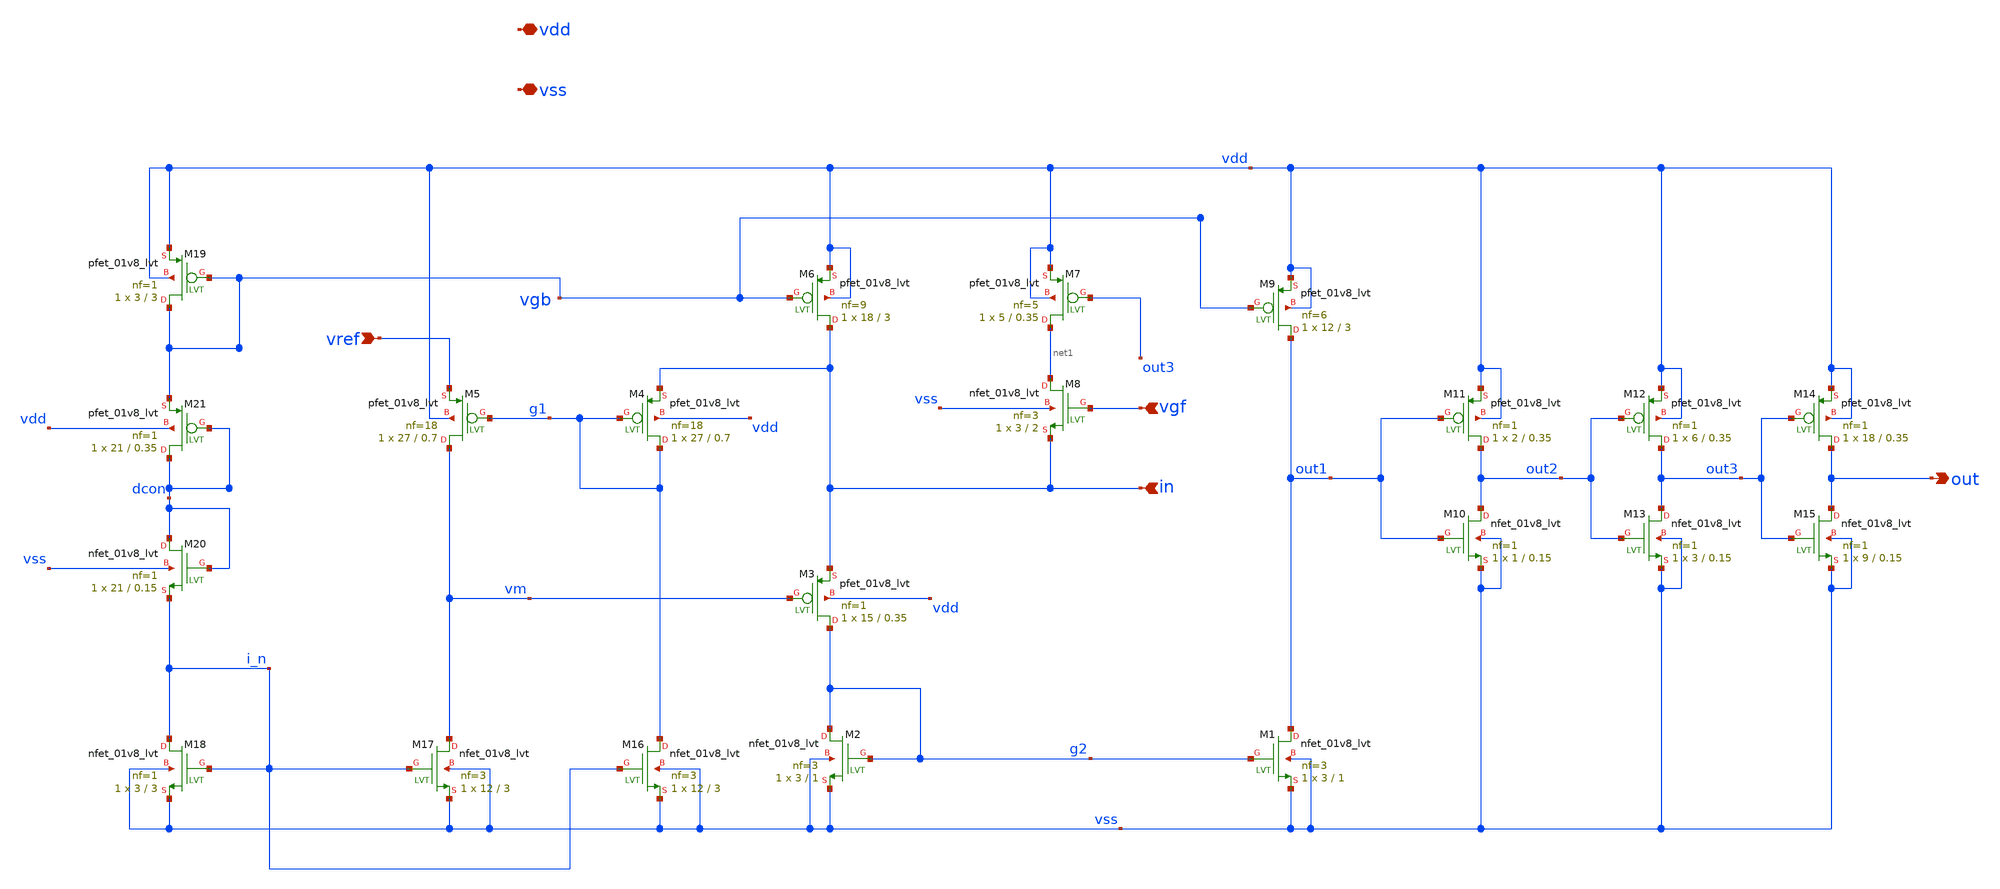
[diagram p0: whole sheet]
** sch_path: xschem/CurrentTrigger.sch
**.subckt CurrentTrigger vdd vss in out vref vgf
*.iopin vdd
*.iopin vss
*.ipin in
*.opin out
*.ipin vref
*.ipin vgf
XM1 out1 g2 vss vss sky130_fd_pr__nfet_01v8_lvt L=1 W=3 nf=3 ad='int((nf+1)/2) * W/nf * 0.29' as='int((nf+2)/2) * W/nf * 0.29'
+ pd='2*int((nf+1)/2) * (W/nf + 0.29)' ps='2*int((nf+2)/2) * (W/nf + 0.29)' nrd='0.29 / W' nrs='0.29 / W'
+ sa=0 sb=0 sd=0 mult=1 m=1
XM2 g2 g2 vss vss sky130_fd_pr__nfet_01v8_lvt L=1 W=3 nf=3 ad='int((nf+1)/2) * W/nf * 0.29' as='int((nf+2)/2) * W/nf * 0.29'
+ pd='2*int((nf+1)/2) * (W/nf + 0.29)' ps='2*int((nf+2)/2) * (W/nf + 0.29)' nrd='0.29 / W' nrs='0.29 / W'
+ sa=0 sb=0 sd=0 mult=1 m=1
XM3 g2 vm in vdd sky130_fd_pr__pfet_01v8_lvt L=0.35 W=15 nf=1 ad='int((nf+1)/2) * W/nf * 0.29' as='int((nf+2)/2) * W/nf * 0.29'
+ pd='2*int((nf+1)/2) * (W/nf + 0.29)' ps='2*int((nf+2)/2) * (W/nf + 0.29)' nrd='0.29 / W' nrs='0.29 / W'
+ sa=0 sb=0 sd=0 mult=1 m=1
XM4 g1 g1 in vdd sky130_fd_pr__pfet_01v8_lvt L=0.7 W=27 nf=18 ad='int((nf+1)/2) * W/nf * 0.29' as='int((nf+2)/2) * W/nf * 0.29'
+ pd='2*int((nf+1)/2) * (W/nf + 0.29)' ps='2*int((nf+2)/2) * (W/nf + 0.29)' nrd='0.29 / W' nrs='0.29 / W'
+ sa=0 sb=0 sd=0 mult=1 m=1
XM5 vm g1 vref vdd sky130_fd_pr__pfet_01v8_lvt L=0.7 W=27 nf=18 ad='int((nf+1)/2) * W/nf * 0.29' as='int((nf+2)/2) * W/nf * 0.29'
+ pd='2*int((nf+1)/2) * (W/nf + 0.29)' ps='2*int((nf+2)/2) * (W/nf + 0.29)' nrd='0.29 / W' nrs='0.29 / W'
+ sa=0 sb=0 sd=0 mult=1 m=1
XM6 in vgb vdd vdd sky130_fd_pr__pfet_01v8_lvt L=3 W=18 nf=9 ad='int((nf+1)/2) * W/nf * 0.29' as='int((nf+2)/2) * W/nf * 0.29'
+ pd='2*int((nf+1)/2) * (W/nf + 0.29)' ps='2*int((nf+2)/2) * (W/nf + 0.29)' nrd='0.29 / W' nrs='0.29 / W'
+ sa=0 sb=0 sd=0 mult=1 m=1
XM7 net1 out3 vdd vdd sky130_fd_pr__pfet_01v8_lvt L=0.35 W=5 nf=5 ad='int((nf+1)/2) * W/nf * 0.29' as='int((nf+2)/2) * W/nf * 0.29'
+ pd='2*int((nf+1)/2) * (W/nf + 0.29)' ps='2*int((nf+2)/2) * (W/nf + 0.29)' nrd='0.29 / W' nrs='0.29 / W'
+ sa=0 sb=0 sd=0 mult=1 m=1
XM9 out1 vgb vdd vdd sky130_fd_pr__pfet_01v8_lvt L=3 W=12 nf=6 ad='int((nf+1)/2) * W/nf * 0.29' as='int((nf+2)/2) * W/nf * 0.29'
+ pd='2*int((nf+1)/2) * (W/nf + 0.29)' ps='2*int((nf+2)/2) * (W/nf + 0.29)' nrd='0.29 / W' nrs='0.29 / W'
+ sa=0 sb=0 sd=0 mult=1 m=1
XM10 out2 out1 vss vss sky130_fd_pr__nfet_01v8_lvt L=0.15 W=1 nf=1 ad='int((nf+1)/2) * W/nf * 0.29' as='int((nf+2)/2) * W/nf * 0.29'
+ pd='2*int((nf+1)/2) * (W/nf + 0.29)' ps='2*int((nf+2)/2) * (W/nf + 0.29)' nrd='0.29 / W' nrs='0.29 / W'
+ sa=0 sb=0 sd=0 mult=1 m=1
XM11 out2 out1 vdd vdd sky130_fd_pr__pfet_01v8_lvt L=0.35 W=2 nf=1 ad='int((nf+1)/2) * W/nf * 0.29' as='int((nf+2)/2) * W/nf * 0.29'
+ pd='2*int((nf+1)/2) * (W/nf + 0.29)' ps='2*int((nf+2)/2) * (W/nf + 0.29)' nrd='0.29 / W' nrs='0.29 / W'
+ sa=0 sb=0 sd=0 mult=1 m=1
XM12 out3 out2 vdd vdd sky130_fd_pr__pfet_01v8_lvt L=0.35 W=6 nf=1 ad='int((nf+1)/2) * W/nf * 0.29' as='int((nf+2)/2) * W/nf * 0.29'
+ pd='2*int((nf+1)/2) * (W/nf + 0.29)' ps='2*int((nf+2)/2) * (W/nf + 0.29)' nrd='0.29 / W' nrs='0.29 / W'
+ sa=0 sb=0 sd=0 mult=1 m=1
XM13 out3 out2 vss vss sky130_fd_pr__nfet_01v8_lvt L=0.15 W=3 nf=1 ad='int((nf+1)/2) * W/nf * 0.29' as='int((nf+2)/2) * W/nf * 0.29'
+ pd='2*int((nf+1)/2) * (W/nf + 0.29)' ps='2*int((nf+2)/2) * (W/nf + 0.29)' nrd='0.29 / W' nrs='0.29 / W'
+ sa=0 sb=0 sd=0 mult=1 m=1
XM14 out out3 vdd vdd sky130_fd_pr__pfet_01v8_lvt L=0.35 W=18 nf=1 ad='int((nf+1)/2) * W/nf * 0.29' as='int((nf+2)/2) * W/nf * 0.29'
+ pd='2*int((nf+1)/2) * (W/nf + 0.29)' ps='2*int((nf+2)/2) * (W/nf + 0.29)' nrd='0.29 / W' nrs='0.29 / W'
+ sa=0 sb=0 sd=0 mult=1 m=1
XM15 out out3 vss vss sky130_fd_pr__nfet_01v8_lvt L=0.15 W=9 nf=1 ad='int((nf+1)/2) * W/nf * 0.29' as='int((nf+2)/2) * W/nf * 0.29'
+ pd='2*int((nf+1)/2) * (W/nf + 0.29)' ps='2*int((nf+2)/2) * (W/nf + 0.29)' nrd='0.29 / W' nrs='0.29 / W'
+ sa=0 sb=0 sd=0 mult=1 m=1
XM16 g1 i_n vss vss sky130_fd_pr__nfet_01v8_lvt L=3 W=12 nf=3 ad='int((nf+1)/2) * W/nf * 0.29' as='int((nf+2)/2) * W/nf * 0.29'
+ pd='2*int((nf+1)/2) * (W/nf + 0.29)' ps='2*int((nf+2)/2) * (W/nf + 0.29)' nrd='0.29 / W' nrs='0.29 / W'
+ sa=0 sb=0 sd=0 mult=1 m=1
XM17 vm i_n vss vss sky130_fd_pr__nfet_01v8_lvt L=3 W=12 nf=3 ad='int((nf+1)/2) * W/nf * 0.29' as='int((nf+2)/2) * W/nf * 0.29'
+ pd='2*int((nf+1)/2) * (W/nf + 0.29)' ps='2*int((nf+2)/2) * (W/nf + 0.29)' nrd='0.29 / W' nrs='0.29 / W'
+ sa=0 sb=0 sd=0 mult=1 m=1
XM18 i_n i_n vss vss sky130_fd_pr__nfet_01v8_lvt L=3 W=3 nf=1 ad='int((nf+1)/2) * W/nf * 0.29' as='int((nf+2)/2) * W/nf * 0.29'
+ pd='2*int((nf+1)/2) * (W/nf + 0.29)' ps='2*int((nf+2)/2) * (W/nf + 0.29)' nrd='0.29 / W' nrs='0.29 / W'
+ sa=0 sb=0 sd=0 mult=1 m=1
XM19 vgb vgb vdd vdd sky130_fd_pr__pfet_01v8_lvt L=3 W=3 nf=1 ad='int((nf+1)/2) * W/nf * 0.29' as='int((nf+2)/2) * W/nf * 0.29'
+ pd='2*int((nf+1)/2) * (W/nf + 0.29)' ps='2*int((nf+2)/2) * (W/nf + 0.29)' nrd='0.29 / W' nrs='0.29 / W'
+ sa=0 sb=0 sd=0 mult=1 m=1
XM20 dcon dcon i_n vss sky130_fd_pr__nfet_01v8_lvt L=0.15 W=21 nf=1 ad='int((nf+1)/2) * W/nf * 0.29'
+ as='int((nf+2)/2) * W/nf * 0.29' pd='2*int((nf+1)/2) * (W/nf + 0.29)' ps='2*int((nf+2)/2) * (W/nf + 0.29)'
+ nrd='0.29 / W' nrs='0.29 / W' sa=0 sb=0 sd=0 mult=1 m=1
XM21 dcon dcon vgb vdd sky130_fd_pr__pfet_01v8_lvt L=0.35 W=21 nf=1 ad='int((nf+1)/2) * W/nf * 0.29'
+ as='int((nf+2)/2) * W/nf * 0.29' pd='2*int((nf+1)/2) * (W/nf + 0.29)' ps='2*int((nf+2)/2) * (W/nf + 0.29)'
+ nrd='0.29 / W' nrs='0.29 / W' sa=0 sb=0 sd=0 mult=1 m=1
XM8 net1 vgf in vss sky130_fd_pr__nfet_01v8_lvt L=2 W=3 nf=3 ad='int((nf+1)/2) * W/nf * 0.29' as='int((nf+2)/2) * W/nf * 0.29'
+ pd='2*int((nf+1)/2) * (W/nf + 0.29)' ps='2*int((nf+2)/2) * (W/nf + 0.29)' nrd='0.29 / W' nrs='0.29 / W'
+ sa=0 sb=0 sd=0 mult=1 m=1
**.ends
.end
